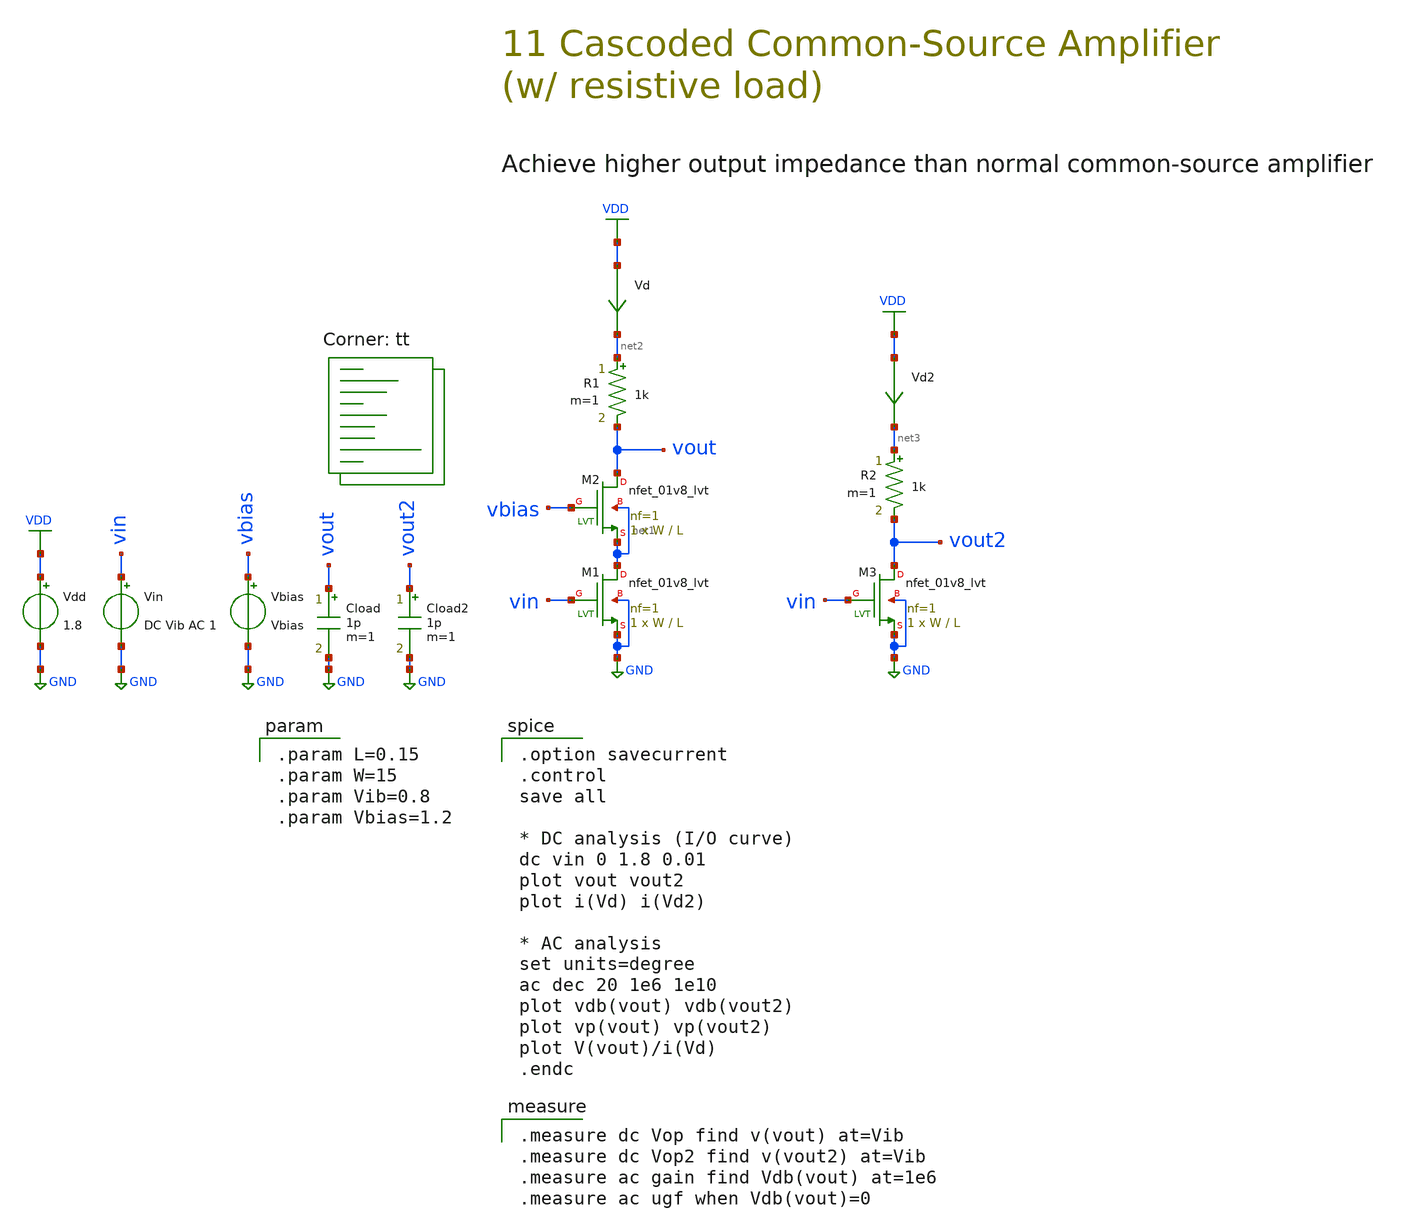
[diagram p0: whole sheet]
** sch_path: 11-a_cascoded-cs.sch
**.subckt 11-a_cascoded-cs
XM1 net1 vin GND GND sky130_fd_pr__nfet_01v8_lvt L=L W=W nf=1 ad='int((1 + 1)/2) * W / 1 * 0.29' as='int((1 + 2)/2) * W / 1 * 0.29'
+ pd='2*int((1 + 1)/2) * (W / 1 + 0.29)' ps='2*int((1 + 2)/2) * (W / 1 + 0.29)' nrd='0.29 / W ' nrs='0.29 / W '
+ sa=0 sb=0 sd=0 mult=1 m=1
Vdd VDD GND 1.8
Vin vin GND DC Vib AC 1
R1 net2 vout 1k m=1
Cload vout GND 1p m=1
XM2 vout vbias net1 net1 sky130_fd_pr__nfet_01v8_lvt L=L W=W nf=1 ad='int((1 + 1)/2) * W / 1 * 0.29'
+ as='int((1 + 2)/2) * W / 1 * 0.29' pd='2*int((1 + 1)/2) * (W / 1 + 0.29)' ps='2*int((1 + 2)/2) * (W / 1 + 0.29)'
+ nrd='0.29 / W ' nrs='0.29 / W ' sa=0 sb=0 sd=0 mult=1 m=1
Vbias vbias GND Vbias
XM3 vout2 vin GND GND sky130_fd_pr__nfet_01v8_lvt L=L W=W nf=1 ad='int((1 + 1)/2) * W / 1 * 0.29' as='int((1 + 2)/2) * W / 1 * 0.29'
+ pd='2*int((1 + 1)/2) * (W / 1 + 0.29)' ps='2*int((1 + 2)/2) * (W / 1 + 0.29)' nrd='0.29 / W ' nrs='0.29 / W '
+ sa=0 sb=0 sd=0 mult=1 m=1
R2 net3 vout2 1k m=1
Cload2 vout2 GND 1p m=1
Vd VDD net2 0
.save i(vd)
Vd2 VDD net3 0
.save i(vd2)
**** begin user architecture code
.lib $::SKYWATER_MODELS/sky130.lib.spice tt

.param L=0.15
.param W=15
.param Vib=0.8
.param Vbias=1.2


.option savecurrent
.control
save all

* DC analysis (I/O curve)
dc vin 0 1.8 0.01
plot vout vout2
plot i(Vd) i(Vd2)

* AC analysis
set units=degree
ac dec 20 1e6 1e10
plot vdb(vout) vdb(vout2)
plot vp(vout) vp(vout2)
plot V(vout)/i(Vd)
.endc


.measure dc Vop find v(vout) at=Vib
.measure dc Vop2 find v(vout2) at=Vib
.measure ac gain find Vdb(vout) at=1e6
.measure ac ugf when Vdb(vout)=0

**** end user architecture code
**.ends
.GLOBAL GND
.GLOBAL VDD
.end
